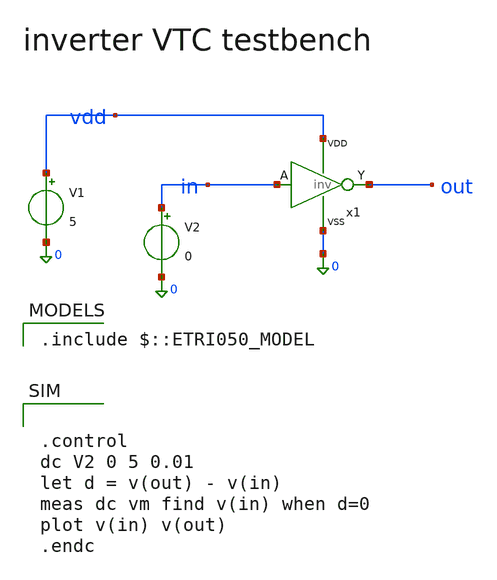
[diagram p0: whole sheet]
** sch_path: sch/inv_tb.sch
**.subckt inv_tb
x1 in out vdd 0 inv
V1 vdd 0 5
V2 in 0 0
**** begin user architecture code

.include $::ETRI050_MODEL



.control
dc V2 0 5 0.01
let d = v(out) - v(in)
meas dc vm find v(in) when d=0
plot v(in) v(out)
.endc


**** end user architecture code
**.ends

* expanding   symbol:  inv.sym # of pins=4
** sym_path: sch/inv.sym
** sch_path: sch/inv.sch
.subckt inv A Y VDD VSS
*.ipin A
*.opin Y
*.iopin VDD
*.iopin VSS
M1 Y A VDD VDD pfet w=3.6u l=0.6u m=1
M2 Y A VSS VSS nfet w=1.8u l=0.6u m=1
.ends

.end
